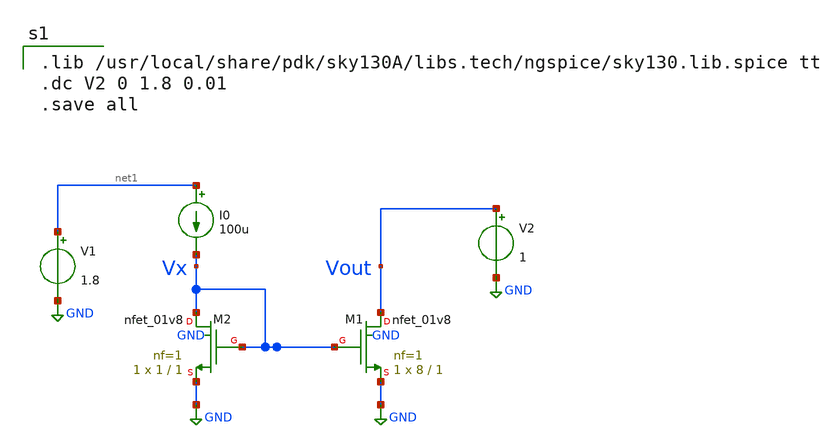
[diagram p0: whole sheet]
** sch_path: Basic_Current_Mirror/current_mirror.sch
**.subckt current_mirror
XM1 Vout Vx GND GND sky130_fd_pr__nfet_01v8 L=1 W=8 nf=1 ad='int((1 + 1)/2) * 8 / 1 * 0.29' as='int((1 + 2)/2) * 8 / 1 * 0.29'
+ pd='2*int((1 + 1)/2) * (8 / 1 + 0.29)' ps='2*int((1 + 2)/2) * (8 / 1 + 0.29)' nrd='0.29 / 8 ' nrs='0.29 / 8 '
+ sa=0 sb=0 sd=0 mult=1 m=1
XM2 Vx Vx GND GND sky130_fd_pr__nfet_01v8 L=1 W=1 nf=1 ad='int((1 + 1)/2) * 1 / 1 * 0.29' as='int((1 + 2)/2) * 1 / 1 * 0.29'
+ pd='2*int((1 + 1)/2) * (1 / 1 + 0.29)' ps='2*int((1 + 2)/2) * (1 / 1 + 0.29)' nrd='0.29 / 1 ' nrs='0.29 / 1 '
+ sa=0 sb=0 sd=0 mult=1 m=1
V1 net1 GND 1.8
V2 Vout GND 1
I0 net1 Vx 100u
**** begin user architecture code

.lib /usr/local/share/pdk/sky130A/libs.tech/ngspice/sky130.lib.spice tt
.dc V2 0 1.8 0.01
.save all


**** end user architecture code
**.ends
.GLOBAL GND
.end
